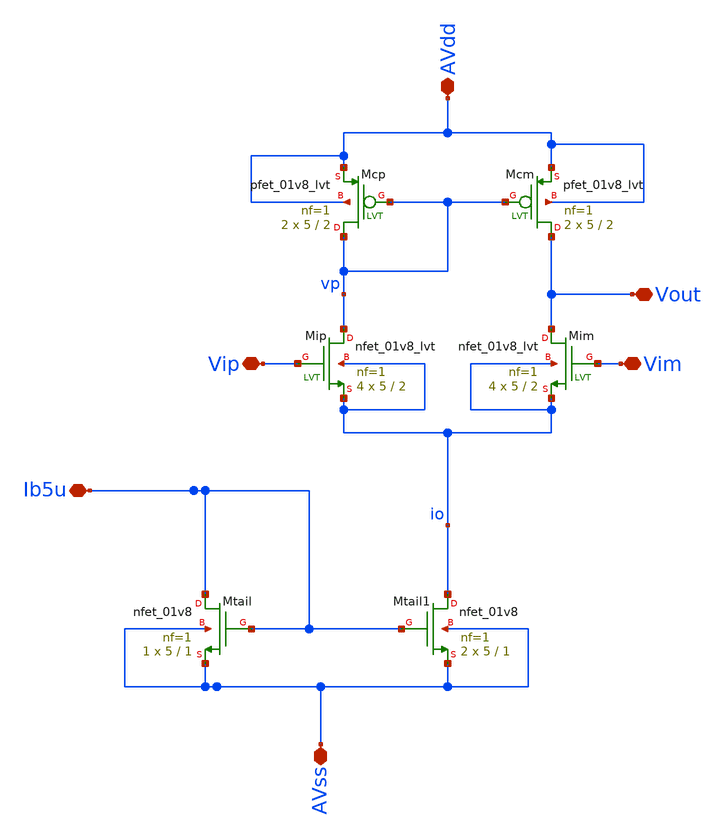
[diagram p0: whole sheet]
** sch_path: Work/xschem/nmos_diff_amp.sch
**.subckt nmos_diff_amp AVdd AVss Vim Vip Vout Ib5u
*.iopin AVdd
*.iopin AVss
*.iopin Vim
*.iopin Vip
*.iopin Vout
*.iopin Ib5u
XMip vp Vip io io sky130_fd_pr__nfet_01v8_lvt L=2 W=5 nf=1 ad='int((1 + 1)/2) * 5 / 1 * 0.29' as='int((1 + 2)/2) * 5 / 1 * 0.29'
+ pd='2*int((1 + 1)/2) * (5 / 1 + 0.29)' ps='2*int((1 + 2)/2) * (5 / 1 + 0.29)' nrd='0.29 / 5 ' nrs='0.29 / 5 '
+ sa=0 sb=0 sd=0 mult=4 m=4
XMim Vout Vim io io sky130_fd_pr__nfet_01v8_lvt L=2 W=5 nf=1 ad='int((1 + 1)/2) * 5 / 1 * 0.29' as='int((1 + 2)/2) * 5 / 1 * 0.29'
+ pd='2*int((1 + 1)/2) * (5 / 1 + 0.29)' ps='2*int((1 + 2)/2) * (5 / 1 + 0.29)' nrd='0.29 / 5 ' nrs='0.29 / 5 '
+ sa=0 sb=0 sd=0 mult=4 m=4
XMcp vp vp AVdd AVdd sky130_fd_pr__pfet_01v8_lvt L=2 W=5 nf=1 ad='int((1 + 1)/2) * 5 / 1 * 0.29' as='int((1 + 2)/2) * 5 / 1 * 0.29'
+ pd='2*int((1 + 1)/2) * (5 / 1 + 0.29)' ps='2*int((1 + 2)/2) * (5 / 1 + 0.29)' nrd='0.29 / 5 ' nrs='0.29 / 5 '
+ sa=0 sb=0 sd=0 mult=2 m=2
XMcm Vout vp AVdd AVdd sky130_fd_pr__pfet_01v8_lvt L=2 W=5 nf=1 ad='int((1 + 1)/2) * 5 / 1 * 0.29' as='int((1 + 2)/2) * 5 / 1 * 0.29'
+ pd='2*int((1 + 1)/2) * (5 / 1 + 0.29)' ps='2*int((1 + 2)/2) * (5 / 1 + 0.29)' nrd='0.29 / 5 ' nrs='0.29 / 5 '
+ sa=0 sb=0 sd=0 mult=2 m=2
XMtail Ib5u Ib5u AVss AVss sky130_fd_pr__nfet_01v8 L=1 W=5 nf=1 ad='int((1 + 1)/2) * 5 / 1 * 0.29' as='int((1 + 2)/2) * 5 / 1 * 0.29'
+ pd='2*int((1 + 1)/2) * (5 / 1 + 0.29)' ps='2*int((1 + 2)/2) * (5 / 1 + 0.29)' nrd='0.29 / 5 ' nrs='0.29 / 5 '
+ sa=0 sb=0 sd=0 mult=1 m=1
XMtail1 io Ib5u AVss AVss sky130_fd_pr__nfet_01v8 L=1 W=5 nf=1 ad='int((1 + 1)/2) * 5 / 1 * 0.29' as='int((1 + 2)/2) * 5 / 1 * 0.29'
+ pd='2*int((1 + 1)/2) * (5 / 1 + 0.29)' ps='2*int((1 + 2)/2) * (5 / 1 + 0.29)' nrd='0.29 / 5 ' nrs='0.29 / 5 '
+ sa=0 sb=0 sd=0 mult=2 m=2
**.ends
.end
